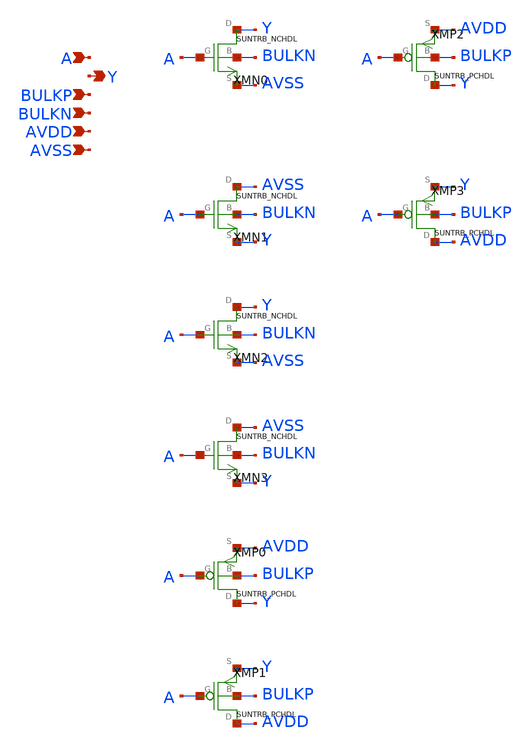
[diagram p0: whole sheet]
** sch_path: ip/sun_trb_sky130nm/design/SUN_TRB_SKY130NM/SUNTRB_IVX4_CV.sch
**.subckt SUNTRB_IVX4_CV A Y BULKP BULKN AVDD AVSS
*.ipin A
*.opin Y
*.ipin BULKP
*.ipin BULKN
*.ipin AVDD
*.ipin AVSS
XMN0 Y A AVSS BULKN SUNTRB_NCHDL xoffset=0 yoffset=0 angle=0
XMN1 AVSS A Y BULKN SUNTRB_NCHDL xoffset=0 yoffset=0 angle=0
XMN2 Y A AVSS BULKN SUNTRB_NCHDL xoffset=0 yoffset=0 angle=0
XMN3 AVSS A Y BULKN SUNTRB_NCHDL xoffset=0 yoffset=0 angle=0
XMP0 Y A AVDD BULKP SUNTRB_PCHDL xoffset=0 yoffset=0 angle=0
XMP1 AVDD A Y BULKP SUNTRB_PCHDL xoffset=0 yoffset=0 angle=0
XMP2 Y A AVDD BULKP SUNTRB_PCHDL xoffset=0 yoffset=0 angle=0
XMP3 AVDD A Y BULKP SUNTRB_PCHDL xoffset=0 yoffset=0 angle=0
**.ends
.end
